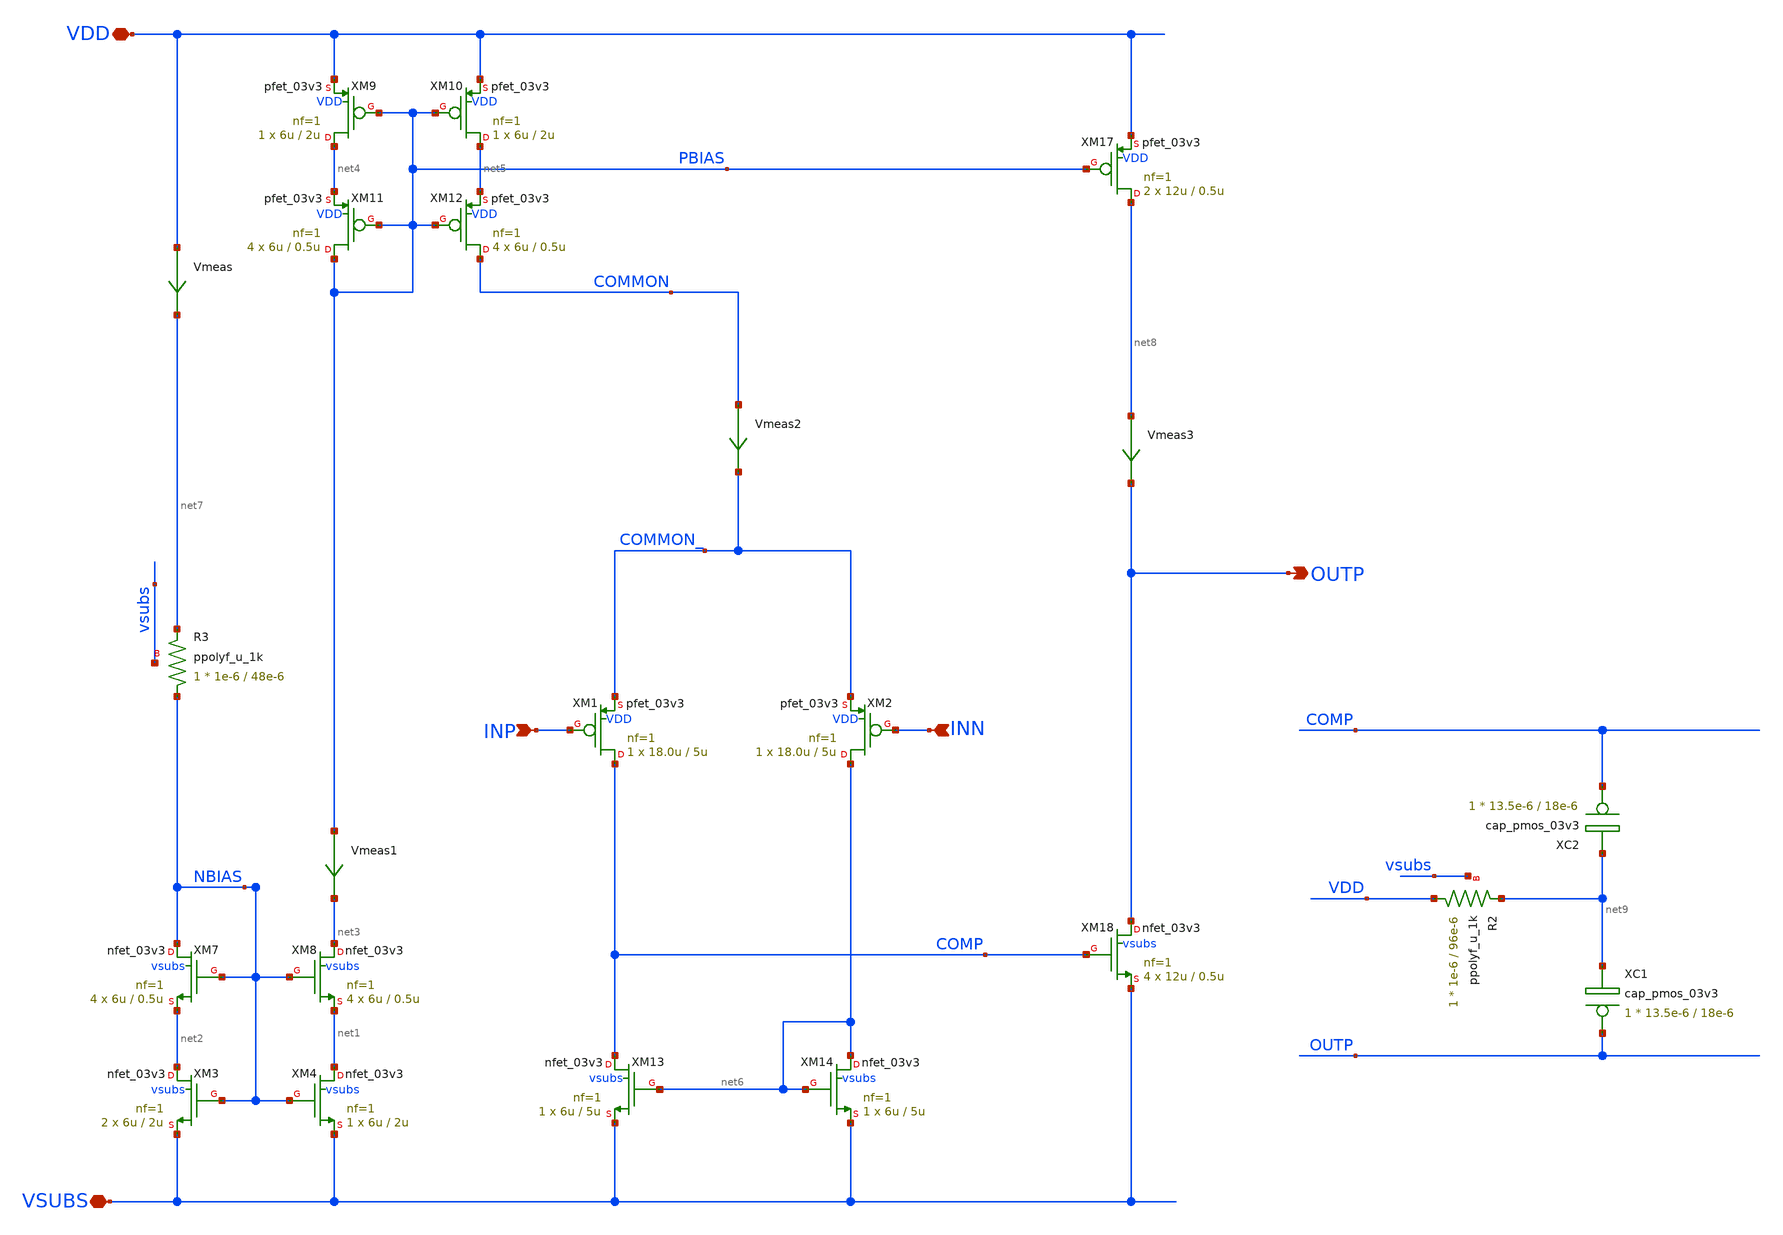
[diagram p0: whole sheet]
** sch_path: xschem/ip_amplifier.sch
**.subckt ip_amplifier VDD VSUBS INP INN OUTP
*.iopin VDD
*.iopin VSUBS
*.ipin INP
*.ipin INN
*.opin OUTP
XM1 COMP INP COMMON_ VDD pfet_03v3 L=5u W=18.0u nf=1 ad='int((nf+1)/2) * W/nf * 0.18u' as='int((nf+2)/2) * W/nf * 0.18u'
+ pd='2*int((nf+1)/2) * (W/nf + 0.18u)' ps='2*int((nf+2)/2) * (W/nf + 0.18u)' nrd='0.18u / W' nrs='0.18u / W'
+ sa=0 sb=0 sd=0 m=1 par=1
XM2 net6 INN COMMON_ VDD pfet_03v3 L=5u W=18.0u nf=1 ad='int((nf+1)/2) * W/nf * 0.18u' as='int((nf+2)/2) * W/nf * 0.18u'
+ pd='2*int((nf+1)/2) * (W/nf + 0.18u)' ps='2*int((nf+2)/2) * (W/nf + 0.18u)' nrd='0.18u / W' nrs='0.18u / W'
+ sa=0 sb=0 sd=0 m=1 par=1
XM3 net2 NBIAS VSUBS vsubs nfet_03v3 L=2u W=6u nf=1 ad='int((nf+1)/2) * W/nf * 0.18u' as='int((nf+2)/2) * W/nf * 0.18u'
+ pd='2*int((nf+1)/2) * (W/nf + 0.18u)' ps='2*int((nf+2)/2) * (W/nf + 0.18u)' nrd='0.18u / W' nrs='0.18u / W'
+ sa=0 sb=0 sd=0 m=2 par=2
XM4 net1 NBIAS VSUBS vsubs nfet_03v3 L=2u W=6u nf=1 ad='int((nf+1)/2) * W/nf * 0.18u' as='int((nf+2)/2) * W/nf * 0.18u'
+ pd='2*int((nf+1)/2) * (W/nf + 0.18u)' ps='2*int((nf+2)/2) * (W/nf + 0.18u)' nrd='0.18u / W' nrs='0.18u / W'
+ sa=0 sb=0 sd=0 m=1 par=1
XM7 NBIAS NBIAS net2 vsubs nfet_03v3 L=0.5u W=6u nf=1 ad='int((nf+1)/2) * W/nf * 0.18u' as='int((nf+2)/2) * W/nf * 0.18u'
+ pd='2*int((nf+1)/2) * (W/nf + 0.18u)' ps='2*int((nf+2)/2) * (W/nf + 0.18u)' nrd='0.18u / W' nrs='0.18u / W'
+ sa=0 sb=0 sd=0 m=4 par=4
XM8 net3 NBIAS net1 vsubs nfet_03v3 L=0.5u W=6u nf=1 ad='int((nf+1)/2) * W/nf * 0.18u' as='int((nf+2)/2) * W/nf * 0.18u'
+ pd='2*int((nf+1)/2) * (W/nf + 0.18u)' ps='2*int((nf+2)/2) * (W/nf + 0.18u)' nrd='0.18u / W' nrs='0.18u / W'
+ sa=0 sb=0 sd=0 m=4 par=4
XM9 net4 PBIAS VDD VDD pfet_03v3 L=2u W=6u nf=1 ad='int((nf+1)/2) * W/nf * 0.18u' as='int((nf+2)/2) * W/nf * 0.18u'
+ pd='2*int((nf+1)/2) * (W/nf + 0.18u)' ps='2*int((nf+2)/2) * (W/nf + 0.18u)' nrd='0.18u / W' nrs='0.18u / W'
+ sa=0 sb=0 sd=0 m=1 par=1
XM10 net5 PBIAS VDD VDD pfet_03v3 L=2u W=6u nf=1 ad='int((nf+1)/2) * W/nf * 0.18u' as='int((nf+2)/2) * W/nf * 0.18u'
+ pd='2*int((nf+1)/2) * (W/nf + 0.18u)' ps='2*int((nf+2)/2) * (W/nf + 0.18u)' nrd='0.18u / W' nrs='0.18u / W'
+ sa=0 sb=0 sd=0 m=1 par=1
XM11 PBIAS PBIAS net4 VDD pfet_03v3 L=0.5u W=6u nf=1 ad='int((nf+1)/2) * W/nf * 0.18u' as='int((nf+2)/2) * W/nf * 0.18u'
+ pd='2*int((nf+1)/2) * (W/nf + 0.18u)' ps='2*int((nf+2)/2) * (W/nf + 0.18u)' nrd='0.18u / W' nrs='0.18u / W'
+ sa=0 sb=0 sd=0 m=4 par=4
XM12 COMMON PBIAS net5 VDD pfet_03v3 L=0.5u W=6u nf=1 ad='int((nf+1)/2) * W/nf * 0.18u' as='int((nf+2)/2) * W/nf * 0.18u'
+ pd='2*int((nf+1)/2) * (W/nf + 0.18u)' ps='2*int((nf+2)/2) * (W/nf + 0.18u)' nrd='0.18u / W' nrs='0.18u / W'
+ sa=0 sb=0 sd=0 m=4 par=4
XM13 COMP net6 VSUBS vsubs nfet_03v3 L=5u W=6u nf=1 ad='int((nf+1)/2) * W/nf * 0.18u' as='int((nf+2)/2) * W/nf * 0.18u'
+ pd='2*int((nf+1)/2) * (W/nf + 0.18u)' ps='2*int((nf+2)/2) * (W/nf + 0.18u)' nrd='0.18u / W' nrs='0.18u / W'
+ sa=0 sb=0 sd=0 m=1 par=1
XM14 net6 net6 VSUBS vsubs nfet_03v3 L=5u W=6u nf=1 ad='int((nf+1)/2) * W/nf * 0.18u' as='int((nf+2)/2) * W/nf * 0.18u'
+ pd='2*int((nf+1)/2) * (W/nf + 0.18u)' ps='2*int((nf+2)/2) * (W/nf + 0.18u)' nrd='0.18u / W' nrs='0.18u / W'
+ sa=0 sb=0 sd=0 m=1 par=1
XM17 net8 PBIAS VDD VDD pfet_03v3 L=0.5u W=12u nf=1 ad='int((nf+1)/2) * W/nf * 0.18u' as='int((nf+2)/2) * W/nf * 0.18u'
+ pd='2*int((nf+1)/2) * (W/nf + 0.18u)' ps='2*int((nf+2)/2) * (W/nf + 0.18u)' nrd='0.18u / W' nrs='0.18u / W'
+ sa=0 sb=0 sd=0 m=2 par=2
XM18 OUTP COMP VSUBS vsubs nfet_03v3 L=0.5u W=12u nf=1 ad='int((nf+1)/2) * W/nf * 0.18u' as='int((nf+2)/2) * W/nf * 0.18u'
+ pd='2*int((nf+1)/2) * (W/nf + 0.18u)' ps='2*int((nf+2)/2) * (W/nf + 0.18u)' nrd='0.18u / W' nrs='0.18u / W'
+ sa=0 sb=0 sd=0 m=4 par=4
XR3 NBIAS net7 vsubs ppolyf_u_1k r_width=1e-6 r_length=48e-6 m=1
Vmeas VDD net7 0
Vmeas1 PBIAS net3 0
XC1 OUTP net9 cap_pmos_03v3 c_width=13.5e-6 c_length=18e-6 m=1
XC2 COMP net9 cap_pmos_03v3 c_width=13.5e-6 c_length=18e-6 m=1
Vmeas2 COMMON COMMON_ 0
Vmeas3 net8 OUTP 0
XR2 VDD net9 vsubs ppolyf_u_1k r_width=1e-6 r_length=96e-6 m=1
**.ends
.end
